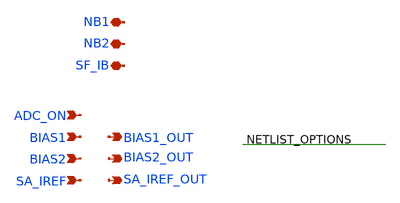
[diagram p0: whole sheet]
** sch_path: xschem/post_layout/bias_layout.sch
**.subckt bias_layout SF_IB NB2 ADC_ON BIAS1 BIAS1_OUT BIAS2 BIAS2_OUT SA_IREF SA_IREF_OUT NB1
*.iopin SF_IB
*.iopin NB2
*.ipin ADC_ON
*.ipin BIAS1
*.opin BIAS1_OUT
*.ipin BIAS2
*.opin BIAS2_OUT
*.ipin SA_IREF
*.opin SA_IREF_OUT
*.iopin NB1
**.ends
**** begin user architecture code


X0 BIAS1 ADC_ON BIAS1_OUT GND sky130_fd_pr__nfet_01v8 ad=2.5e+12p pd=1.1e+07u as=5.9425e+12p
+ ps=1.514e+07u w=5e+06u l=1e+06u
X1 NB1 NB1 GND GND sky130_fd_pr__nfet_01v8_lvt ad=3.5e+11p pd=2.7e+06u as=1.272e+13p ps=4.894e+07u
+ w=1e+06u l=1.2e+06u
X2 BIAS2_OUT BIAS2_OUT GND GND sky130_fd_pr__nfet_01v8_lvt ad=5.9725e+12p pd=1.52e+07u as=0p ps=0u
+ w=1e+06u l=1e+06u
X3 SA_IREF_OUT SA_IREF_OUT GND GND sky130_fd_pr__nfet_01v8 ad=5.9905e+12p pd=1.53e+07u as=0p ps=0u
+ w=500000u l=1e+06u
X4 NB2 NB2 GND GND sky130_fd_pr__nfet_01v8_lvt ad=3.5e+11p pd=2.7e+06u as=0p ps=0u w=1e+06u
+ l=1.2e+06u
X5 BIAS2 ADC_ON BIAS2_OUT GND sky130_fd_pr__nfet_01v8 ad=2.5e+12p pd=1.1e+07u as=0p ps=0u w=5e+06u
+ l=1e+06u
X6 AMP_IB AMP_IB GND GND sky130_fd_pr__nfet_01v8_lvt ad=5.6e+12p pd=1.74e+07u as=0p ps=0u w=8e+06u
+ l=2e+06u
X7 OUT_IB OUT_IB GND GND sky130_fd_pr__nfet_01v8_lvt ad=5.6e+12p pd=1.74e+07u as=0p ps=0u w=8e+06u
+ l=2e+06u
X8 SA_IREF ADC_ON SA_IREF_OUT GND sky130_fd_pr__nfet_01v8 ad=2.5e+12p pd=1.1e+07u as=0p ps=0u
+ w=5e+06u l=1e+06u
X9 BIAS1_OUT BIAS1_OUT GND GND sky130_fd_pr__nfet_01v8 ad=0p pd=0u as=0p ps=0u w=420000u l=1e+06u
X10 SF_IB SF_IB VDD VDD sky130_fd_pr__pfet_01v8_lvt ad=5.5e+11p pd=3.1e+06u as=4.5e+11p ps=2.9e+06u
+ w=1e+06u l=1e+06u




**** end user architecture code
.end
